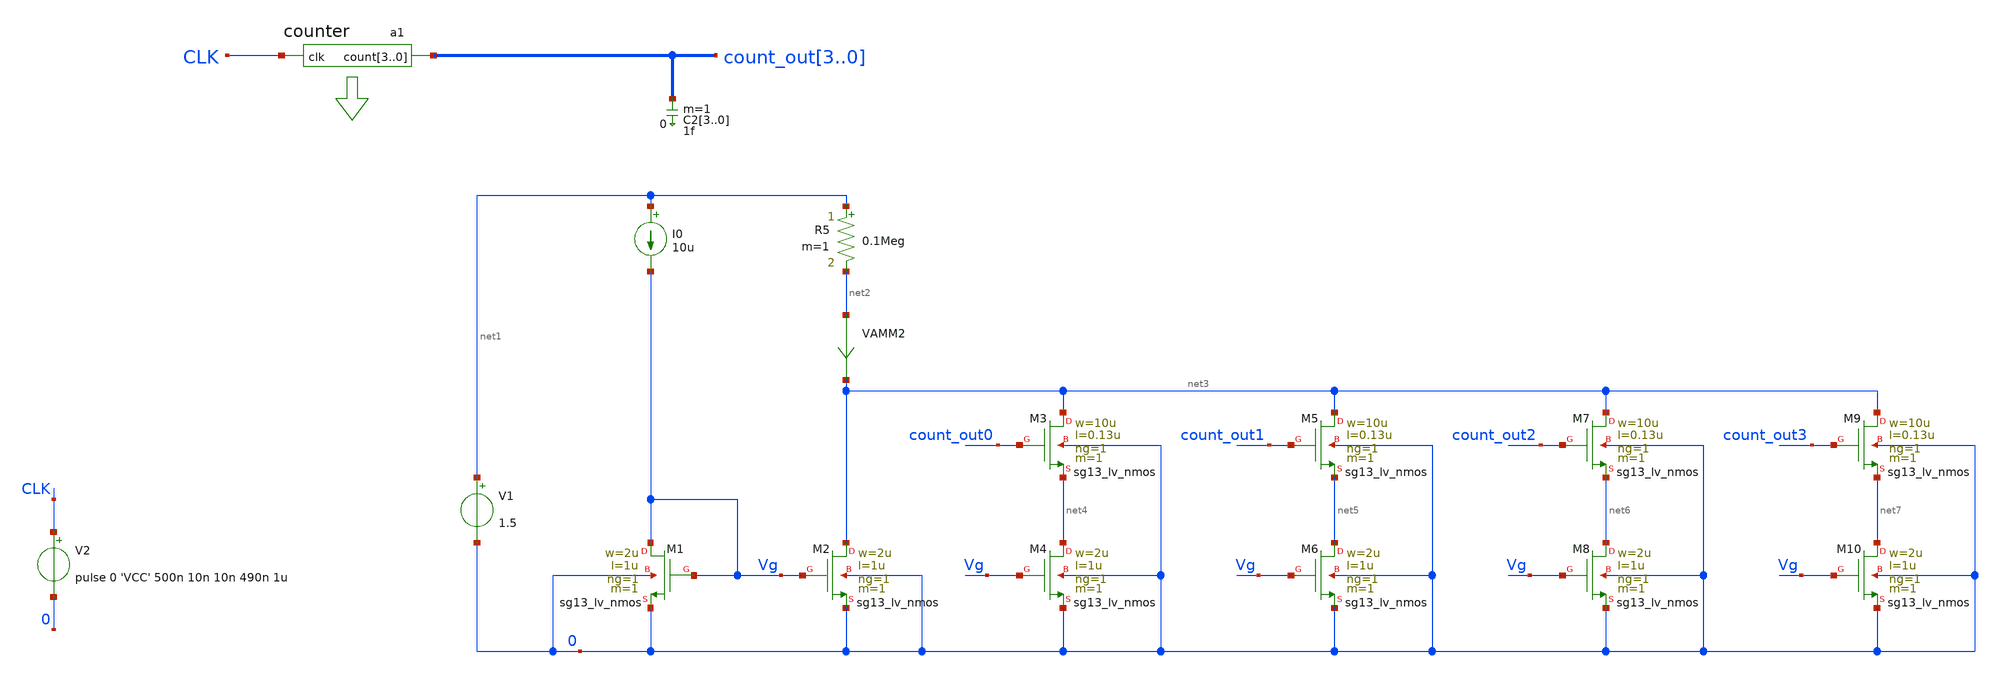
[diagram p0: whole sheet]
** sch_path: xschem/current_mirror_cosim.sch
**.subckt current_mirror_cosim
C23 count_out3 0 1f m=1
C22 count_out2 0 1f m=1
C21 count_out1 0 1f m=1
C20 count_out0 0 1f m=1
a1 [ CLK ] [ count_out3 count_out2 count_out1 count_out0 ] counter
V2 CLK 0 pulse 0 'VCC' 500n 10n 10n 490n 1u
XM1 Vg Vg 0 0 sg13_lv_nmos w=2u l=1u ng=1 m=1 mm_ok=1
I0 net1 Vg 10u
V1 net1 0 1.5
XM2 net3 Vg 0 0 sg13_lv_nmos w=2u l=1u ng=1 m=1 mm_ok=1
R5 net1 net2 0.1Meg m=1
VAMM2 net2 net3 0
XM3 net3 count_out0 net4 0 sg13_lv_nmos w=10u l=0.13u ng=1 m=1 mm_ok=1
XM4 net4 Vg 0 0 sg13_lv_nmos w=2u l=1u ng=1 m=1 mm_ok=1
XM5 net3 count_out1 net5 0 sg13_lv_nmos w=10u l=0.13u ng=1 m=1 mm_ok=1
XM6 net5 Vg 0 0 sg13_lv_nmos w=2u l=1u ng=1 m=1 mm_ok=1
XM7 net3 count_out2 net6 0 sg13_lv_nmos w=10u l=0.13u ng=1 m=1 mm_ok=1
XM8 net6 Vg 0 0 sg13_lv_nmos w=2u l=1u ng=1 m=1 mm_ok=1
XM9 net3 count_out3 net7 0 sg13_lv_nmos w=10u l=0.13u ng=1 m=1 mm_ok=1
XM10 net7 Vg 0 0 sg13_lv_nmos w=2u l=1u ng=1 m=1 mm_ok=1
**** begin user architecture code


.temp 27

.option method=gear
.param VCC=1.5

.control
save all
tran 0.1n 50u
*set wr_singlescale
*set wr_vecnames
*option numdgt=4
*plot i(Vmeas) i(Vmeas1)
remzerovec
write current_mirror_cosim.raw

.endc


 .lib cornerMOSlv.lib mos_tt

**** end user architecture code
**.ends
**** begin user architecture code
.model counter d_cosim simulation="ivlng" sim_args=["counter"] delay=0
**** end user architecture code
.end
